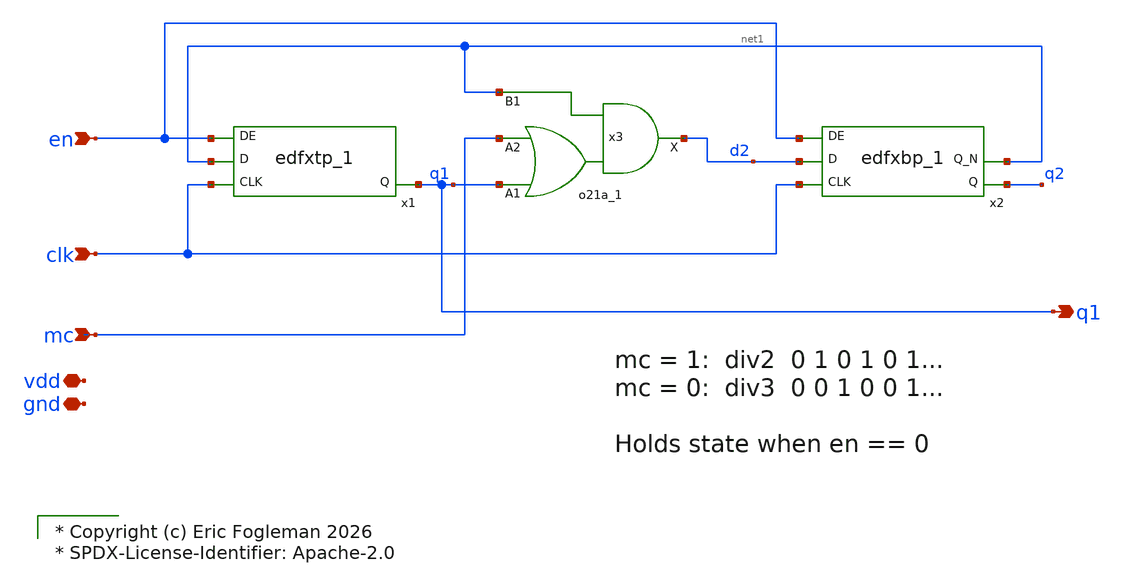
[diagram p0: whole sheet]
** sch_path: xschem/ejf_pll96_sdiv23.sch

* Copyright (c) Eric Fogleman 2026
* SPDX-License-Identifier: Apache-2.0

**.subckt ejf_pll96_sdiv23 clk mc q1 vdd gnd en
*.ipin clk
*.ipin mc
*.opin q1
*.iopin vdd
*.iopin gnd
*.ipin en
x3 q1 mc net1 gnd gnd vdd vdd d2 sky130_fd_sc_ls__o21a_1
x1 clk net1 en gnd gnd vdd vdd q1 sky130_fd_sc_ls__edfxtp_1
x2 clk d2 en gnd gnd vdd vdd q2 net1 sky130_fd_sc_ls__edfxbp_1
**.ends
.end
